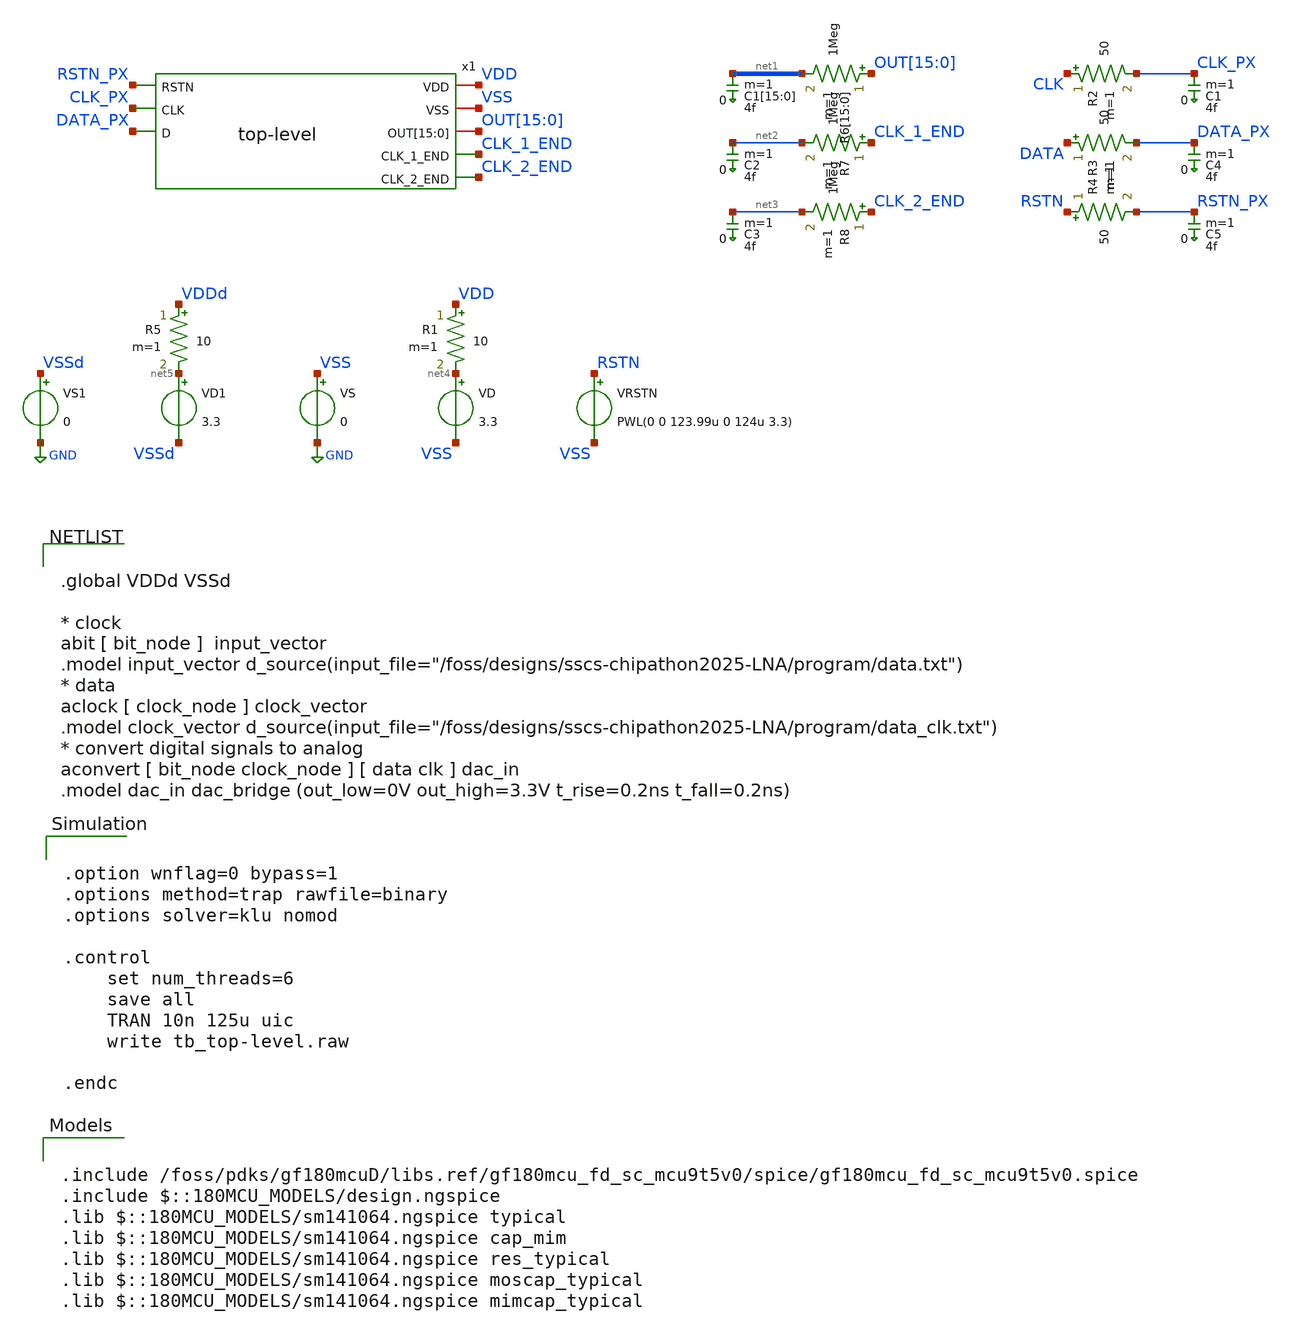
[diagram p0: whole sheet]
** sch_path: designs/libs/tb_top-level/tb_top-level.sch
**.subckt tb_top-level
VD net4 VSS 3.3
R1 VDD net4 10 m=1
R2 CLK CLK_PX 50 m=1
R3 DATA DATA_PX 50 m=1
VS VSS GND 0
VRSTN RSTN VSS PWL(0 0 123.99u 0 124u 3.3)
R4 RSTN RSTN_PX 50 m=1
VD1 net5 VSSd 3.3
R5 VDDd net5 10 m=1
VS1 VSSd GND 0
C1[15] net1[15] 0 4f m=1
C1[14] net1[14] 0 4f m=1
C1[13] net1[13] 0 4f m=1
C1[12] net1[12] 0 4f m=1
C1[11] net1[11] 0 4f m=1
C1[10] net1[10] 0 4f m=1
C1[9] net1[9] 0 4f m=1
C1[8] net1[8] 0 4f m=1
C1[7] net1[7] 0 4f m=1
C1[6] net1[6] 0 4f m=1
C1[5] net1[5] 0 4f m=1
C1[4] net1[4] 0 4f m=1
C1[3] net1[3] 0 4f m=1
C1[2] net1[2] 0 4f m=1
C1[1] net1[1] 0 4f m=1
C1[0] net1[0] 0 4f m=1
C2 net2 0 4f m=1
C3 net3 0 4f m=1
C1 CLK_PX 0 4f m=1
C4 DATA_PX 0 4f m=1
R6[15] OUT[15] net1[15] 1Meg m=1
R6[14] OUT[14] net1[14] 1Meg m=1
R6[13] OUT[13] net1[13] 1Meg m=1
R6[12] OUT[12] net1[12] 1Meg m=1
R6[11] OUT[11] net1[11] 1Meg m=1
R6[10] OUT[10] net1[10] 1Meg m=1
R6[9] OUT[9] net1[9] 1Meg m=1
R6[8] OUT[8] net1[8] 1Meg m=1
R6[7] OUT[7] net1[7] 1Meg m=1
R6[6] OUT[6] net1[6] 1Meg m=1
R6[5] OUT[5] net1[5] 1Meg m=1
R6[4] OUT[4] net1[4] 1Meg m=1
R6[3] OUT[3] net1[3] 1Meg m=1
R6[2] OUT[2] net1[2] 1Meg m=1
R6[1] OUT[1] net1[1] 1Meg m=1
R6[0] OUT[0] net1[0] 1Meg m=1
R7 CLK_1_END net2 1Meg m=1
R8 CLK_2_END net3 1Meg m=1
C5 RSTN_PX 0 4f m=1
x1 VDD VSS OUT[15] OUT[14] OUT[13] OUT[12] OUT[11] OUT[10] OUT[9] OUT[8] OUT[7] OUT[6] OUT[5] OUT[4]
+ OUT[3] OUT[2] OUT[1] OUT[0] RSTN_PX CLK_PX DATA_PX CLK_1_END CLK_2_END top-level
**** begin user architecture code


.option wnflag=0 bypass=1
.options method=trap rawfile=binary
.options solver=klu nomod

.control
    set num_threads=6
    save all
    TRAN 10n 125u uic
    write tb_top-level.raw

.endc



.include /foss/pdks/gf180mcuD/libs.ref/gf180mcu_fd_sc_mcu9t5v0/spice/gf180mcu_fd_sc_mcu9t5v0.spice
.include $::180MCU_MODELS/design.ngspice
.lib $::180MCU_MODELS/sm141064.ngspice typical
.lib $::180MCU_MODELS/sm141064.ngspice cap_mim
.lib $::180MCU_MODELS/sm141064.ngspice res_typical
.lib $::180MCU_MODELS/sm141064.ngspice moscap_typical
.lib $::180MCU_MODELS/sm141064.ngspice mimcap_typical



.global VDDd VSSd

* clock
abit [ bit_node ]  input_vector
.model input_vector d_source(input_file="/foss/designs/sscs-chipathon2025-LNA/program/data.txt")
* data
aclock [ clock_node ] clock_vector
.model clock_vector d_source(input_file="/foss/designs/sscs-chipathon2025-LNA/program/data_clk.txt")
* convert digital signals to analog
aconvert [ bit_node clock_node ] [ data clk ] dac_in
.model dac_in dac_bridge (out_low=0V out_high=3.3V t_rise=0.2ns t_fall=0.2ns)


**** end user architecture code
**.ends
.GLOBAL GND
.end
